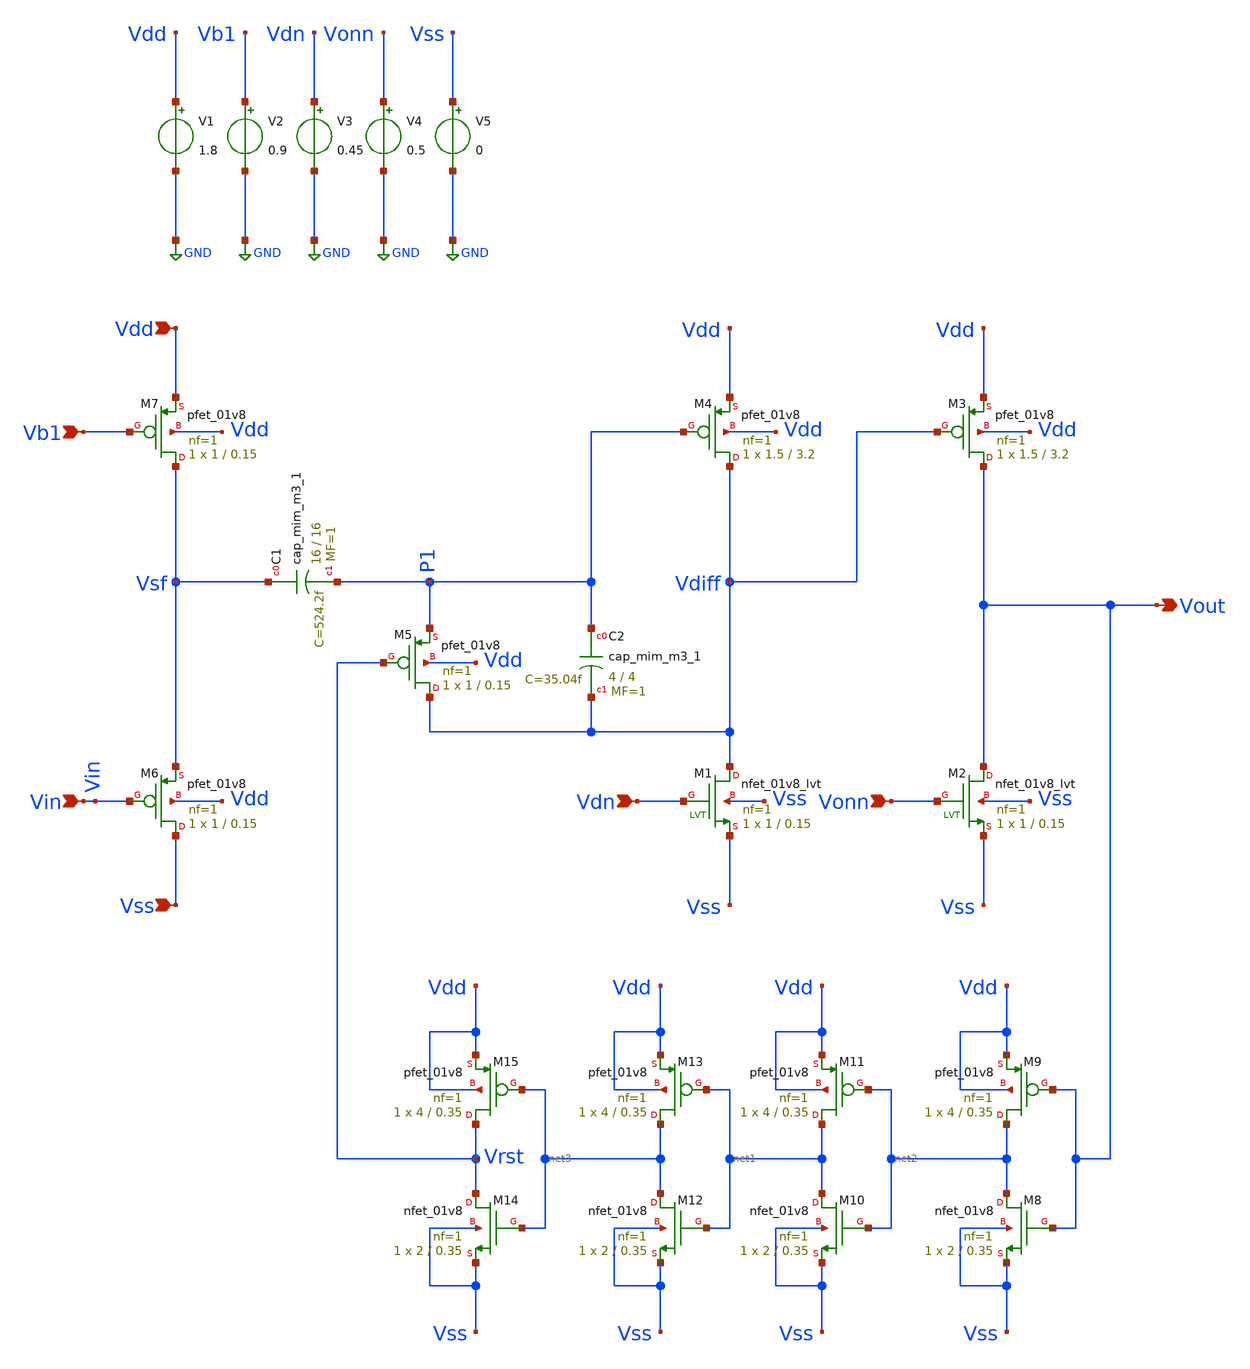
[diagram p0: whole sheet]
** sch_path: testbenches/AnalogToSpike_tb.sch
**.subckt AnalogToSpike_tb Vdd Vss Vdn Vonn Vb1 Vin Vout
*.ipin Vdd
*.ipin Vss
*.ipin Vdn
*.ipin Vonn
*.ipin Vb1
*.ipin Vin
*.opin Vout
XM3 Vout Vdiff Vdd Vdd sky130_fd_pr__pfet_01v8 L=3.2 W=1.5 nf=1 ad='int((nf+1)/2) * W/nf * 0.29' as='int((nf+2)/2) * W/nf * 0.29'
+ pd='2*int((nf+1)/2) * (W/nf + 0.29)' ps='2*int((nf+2)/2) * (W/nf + 0.29)' nrd='0.29 / W' nrs='0.29 / W'
+ sa=0 sb=0 sd=0 mult=1 m=1
XM4 Vdiff P1 Vdd Vdd sky130_fd_pr__pfet_01v8 L=3.2 W=1.5 nf=1 ad='int((nf+1)/2) * W/nf * 0.29' as='int((nf+2)/2) * W/nf * 0.29'
+ pd='2*int((nf+1)/2) * (W/nf + 0.29)' ps='2*int((nf+2)/2) * (W/nf + 0.29)' nrd='0.29 / W' nrs='0.29 / W'
+ sa=0 sb=0 sd=0 mult=1 m=1
XM5 Vdiff Vrst P1 Vdd sky130_fd_pr__pfet_01v8 L=0.15 W=1 nf=1 ad='int((nf+1)/2) * W/nf * 0.29' as='int((nf+2)/2) * W/nf * 0.29'
+ pd='2*int((nf+1)/2) * (W/nf + 0.29)' ps='2*int((nf+2)/2) * (W/nf + 0.29)' nrd='0.29 / W' nrs='0.29 / W'
+ sa=0 sb=0 sd=0 mult=1 m=1
XM6 Vss Vin Vsf Vdd sky130_fd_pr__pfet_01v8 L=0.15 W=1 nf=1 ad='int((nf+1)/2) * W/nf * 0.29' as='int((nf+2)/2) * W/nf * 0.29'
+ pd='2*int((nf+1)/2) * (W/nf + 0.29)' ps='2*int((nf+2)/2) * (W/nf + 0.29)' nrd='0.29 / W' nrs='0.29 / W'
+ sa=0 sb=0 sd=0 mult=1 m=1
XM7 Vsf Vb1 Vdd Vdd sky130_fd_pr__pfet_01v8 L=0.15 W=1 nf=1 ad='int((nf+1)/2) * W/nf * 0.29' as='int((nf+2)/2) * W/nf * 0.29'
+ pd='2*int((nf+1)/2) * (W/nf + 0.29)' ps='2*int((nf+2)/2) * (W/nf + 0.29)' nrd='0.29 / W' nrs='0.29 / W'
+ sa=0 sb=0 sd=0 mult=1 m=1
XC1 Vsf P1 sky130_fd_pr__cap_mim_m3_1 W=16 L=16 MF=1 m=1
XC2 P1 Vdiff sky130_fd_pr__cap_mim_m3_1 W=4 L=4 MF=1 m=1
V1 Vdd GND 1.8
V2 Vb1 GND 0.9
V3 Vdn GND 0.45
V4 Vonn GND 0.5
V5 Vss GND 0
XM1 Vdiff Vdn Vss Vss sky130_fd_pr__nfet_01v8_lvt L=0.15 W=1 nf=1 ad='int((nf+1)/2) * W/nf * 0.29' as='int((nf+2)/2) * W/nf * 0.29'
+ pd='2*int((nf+1)/2) * (W/nf + 0.29)' ps='2*int((nf+2)/2) * (W/nf + 0.29)' nrd='0.29 / W' nrs='0.29 / W'
+ sa=0 sb=0 sd=0 mult=1 m=1
XM2 Vout Vonn Vss Vss sky130_fd_pr__nfet_01v8_lvt L=0.15 W=1 nf=1 ad='int((nf+1)/2) * W/nf * 0.29' as='int((nf+2)/2) * W/nf * 0.29'
+ pd='2*int((nf+1)/2) * (W/nf + 0.29)' ps='2*int((nf+2)/2) * (W/nf + 0.29)' nrd='0.29 / W' nrs='0.29 / W'
+ sa=0 sb=0 sd=0 mult=1 m=1
XM8 net2 Vout Vss Vss sky130_fd_pr__nfet_01v8 L=0.35 W=2 nf=1 ad='int((nf+1)/2) * W/nf * 0.29' as='int((nf+2)/2) * W/nf * 0.29'
+ pd='2*int((nf+1)/2) * (W/nf + 0.29)' ps='2*int((nf+2)/2) * (W/nf + 0.29)' nrd='0.29 / W' nrs='0.29 / W'
+ sa=0 sb=0 sd=0 mult=1 m=1
XM9 net2 Vout Vdd Vdd sky130_fd_pr__pfet_01v8 L=0.35 W=4 nf=1 ad='int((nf+1)/2) * W/nf * 0.29' as='int((nf+2)/2) * W/nf * 0.29'
+ pd='2*int((nf+1)/2) * (W/nf + 0.29)' ps='2*int((nf+2)/2) * (W/nf + 0.29)' nrd='0.29 / W' nrs='0.29 / W'
+ sa=0 sb=0 sd=0 mult=1 m=1
XM10 net1 net2 Vss Vss sky130_fd_pr__nfet_01v8 L=0.35 W=2 nf=1 ad='int((nf+1)/2) * W/nf * 0.29' as='int((nf+2)/2) * W/nf * 0.29'
+ pd='2*int((nf+1)/2) * (W/nf + 0.29)' ps='2*int((nf+2)/2) * (W/nf + 0.29)' nrd='0.29 / W' nrs='0.29 / W'
+ sa=0 sb=0 sd=0 mult=1 m=1
XM11 net1 net2 Vdd Vdd sky130_fd_pr__pfet_01v8 L=0.35 W=4 nf=1 ad='int((nf+1)/2) * W/nf * 0.29' as='int((nf+2)/2) * W/nf * 0.29'
+ pd='2*int((nf+1)/2) * (W/nf + 0.29)' ps='2*int((nf+2)/2) * (W/nf + 0.29)' nrd='0.29 / W' nrs='0.29 / W'
+ sa=0 sb=0 sd=0 mult=1 m=1
XM12 net3 net1 Vss Vss sky130_fd_pr__nfet_01v8 L=0.35 W=2 nf=1 ad='int((nf+1)/2) * W/nf * 0.29' as='int((nf+2)/2) * W/nf * 0.29'
+ pd='2*int((nf+1)/2) * (W/nf + 0.29)' ps='2*int((nf+2)/2) * (W/nf + 0.29)' nrd='0.29 / W' nrs='0.29 / W'
+ sa=0 sb=0 sd=0 mult=1 m=1
XM13 net3 net1 Vdd Vdd sky130_fd_pr__pfet_01v8 L=0.35 W=4 nf=1 ad='int((nf+1)/2) * W/nf * 0.29' as='int((nf+2)/2) * W/nf * 0.29'
+ pd='2*int((nf+1)/2) * (W/nf + 0.29)' ps='2*int((nf+2)/2) * (W/nf + 0.29)' nrd='0.29 / W' nrs='0.29 / W'
+ sa=0 sb=0 sd=0 mult=1 m=1
XM14 Vrst net3 Vss Vss sky130_fd_pr__nfet_01v8 L=0.35 W=2 nf=1 ad='int((nf+1)/2) * W/nf * 0.29' as='int((nf+2)/2) * W/nf * 0.29'
+ pd='2*int((nf+1)/2) * (W/nf + 0.29)' ps='2*int((nf+2)/2) * (W/nf + 0.29)' nrd='0.29 / W' nrs='0.29 / W'
+ sa=0 sb=0 sd=0 mult=1 m=1
XM15 Vrst net3 Vdd Vdd sky130_fd_pr__pfet_01v8 L=0.35 W=4 nf=1 ad='int((nf+1)/2) * W/nf * 0.29' as='int((nf+2)/2) * W/nf * 0.29'
+ pd='2*int((nf+1)/2) * (W/nf + 0.29)' ps='2*int((nf+2)/2) * (W/nf + 0.29)' nrd='0.29 / W' nrs='0.29 / W'
+ sa=0 sb=0 sd=0 mult=1 m=1
**** begin user architecture code

** opencircuitdesign pdks install
.lib $::SKYWATER_MODELS/sky130.lib.spice tt





.option savecurrents
.temp 27

* Case #1 -> 100 Hz
Vin vin 0 SIN(0 0.3 100 0 0)
*Vreset vreset 0 PULSE(1.8 0 0 1u 1u 900u 1000u)

* Case #2 -> 10 Hz
*Vin vin 0 SIN(0 0.3 10 0 0)
*Vreset vreset 0 PULSE(1.8 0 0 100u 100u 9m 10m)

* Case #3 -> 1 Hz
*Vin vin 0 SIN(0 0.3 1 0 0)
*Vreset vreset 0 PULSE(1.8 0 0 1m 1m 90m 100m)

.control
save all
*op

* Case #1 -> Run 40 ms
tran 1u 0.04

* Case #2 -> Run 400 ms
*tran 100u 0.4

* Case #3 -> Run 4 s
*tran 1m 4

plot vin vout

write ATS_version_0.0.raw

.endc



**** end user architecture code
**.ends
.GLOBAL GND
.end
